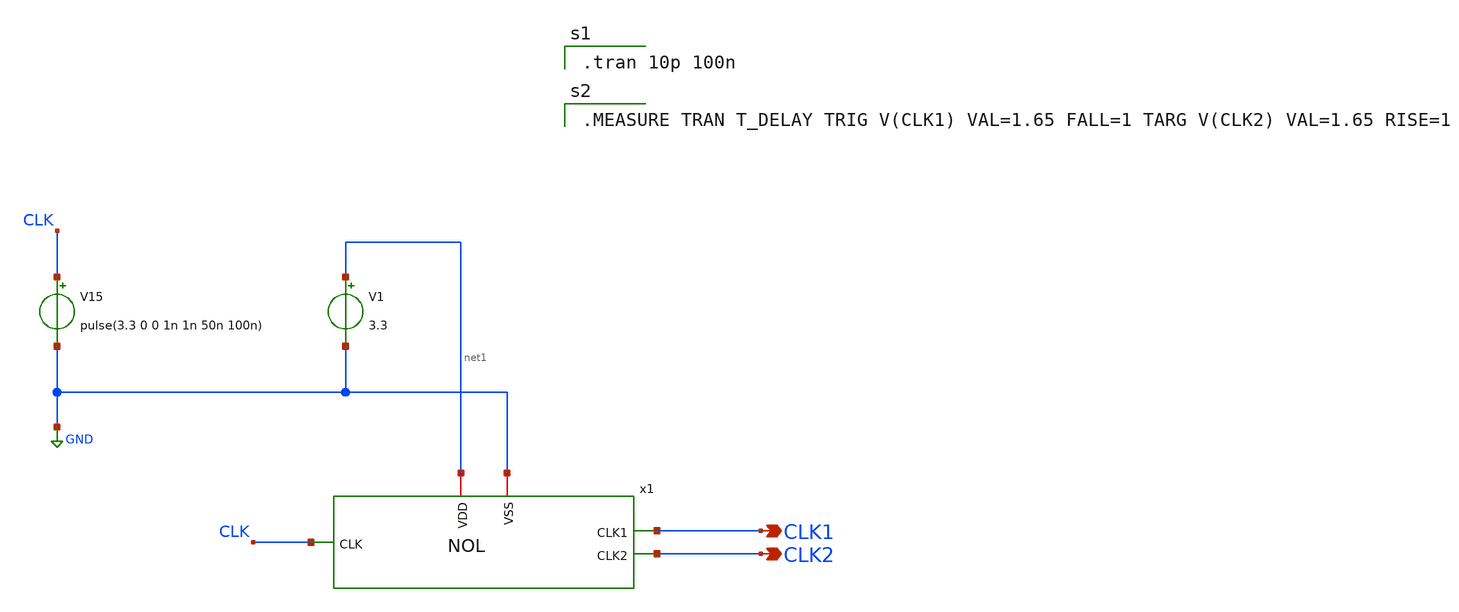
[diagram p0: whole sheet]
** sch_path: NOL_sim.sch
**.subckt NOL_sim CLK1 CLK2
*.opin CLK1
*.opin CLK2
x1 net1 CLK CLK1 GND CLK2 NOL
V15 CLK GND pulse(3.3 0 0 1n 1n 50n 100n)
V1 net1 GND 3.3
**** begin user architecture code

.tran 10p 100n


.MEASURE TRAN T_DELAY TRIG V(CLK1) VAL=1.65 FALL=1 TARG V(CLK2) VAL=1.65 RISE=1

**** end user architecture code
**.ends

* expanding   symbol:  C:/Users/ISLab2/Documents/minimal_LR/NOL.sym # of pins=5
** sym_path: NOL.sym
** sch_path: NOL.sch
.subckt NOL VDD CLK CLK1 VSS CLK2
*.ipin CLK
*.opin CLK1
*.opin CLK2
*.iopin VDD
*.iopin VSS
x3 VDD net1 CLK VSS INV
x1 VDD CLK net9 CLK2 VSS NOR
x2 VDD CLK1 net2 net1 VSS NOR
x4 VDD net3 net2 VSS INV
x5 VDD net4 net3 VSS INV
x6 VDD net5 net4 VSS INV
x7 VDD net17 net5 VSS INV
x8 VDD net6 net9 VSS INV
x9 VDD net7 net6 VSS INV
x10 VDD net8 net7 VSS INV
x11 VDD net13 net8 VSS INV
x12 VDD net10 net13 VSS INV
x13 VDD net11 net10 VSS INV
x14 VDD net12 net11 VSS INV
x15 VDD net32 net12 VSS INV
x16 VDD net14 net17 VSS INV
x17 VDD net15 net14 VSS INV
x18 VDD net16 net15 VSS INV
x19 VDD net33 net16 VSS INV
x20 VDD net18 net33 VSS INV
x21 VDD net19 net18 VSS INV
x22 VDD net20 net19 VSS INV
x23 VDD net24 net20 VSS INV
x24 VDD net21 net24 VSS INV
x25 VDD net22 net21 VSS INV
x26 VDD net23 net22 VSS INV
x27 VDD CLK2 net23 VSS INV
x28 VDD net25 net32 VSS INV
x29 VDD net26 net25 VSS INV
x30 VDD net27 net26 VSS INV
x31 VDD net31 net27 VSS INV
x32 VDD net28 net31 VSS INV
x33 VDD net29 net28 VSS INV
x34 VDD net30 net29 VSS INV
x35 VDD CLK1 net30 VSS INV
.ends


* expanding   symbol:  C:/Users/ISLab2/Documents/minimal_LR/INV.sym # of pins=4
** sym_path: INV.sym
** sch_path: INV.sch
.subckt INV VDD OUT IN VSS
*.opin OUT
*.ipin IN
*.iopin VDD
*.iopin VSS
M2 OUT IN VDD VDD pch w=10u l=0.35u as=0 ps=0 ad=0 pd=0 m=1
M1 OUT IN VSS VSS nch w=5u l=0.35u as=0 ps=0 ad=0 pd=0 m=1
.ends


* expanding   symbol:  C:/Users/ISLab2/Documents/minimal_LR/NOR.sym # of pins=5
** sym_path: NOR.sym
** sch_path: NOR.sch
.subckt NOR VDD A Y B VSS
*.iopin VDD
*.ipin A
*.ipin B
*.iopin VSS
*.opin Y
M1 Y A VSS VSS nch w=3.5u l=0.35u as=0 ps=0 ad=0 pd=0 m=1
M2 net1 A VDD VDD pch w=3.5u l=0.35u as=0 ps=0 ad=0 pd=0 m=1
M3 Y B net1 VDD pch w=3.5u l=0.35u as=0 ps=0 ad=0 pd=0 m=1
M4 Y B VSS VSS nch w=3.5u l=0.35u as=0 ps=0 ad=0 pd=0 m=1
**** begin user architecture code


.include C:/Users/ISLab2/Documents/minimal_LR/minimal.txt

**** end user architecture code
.ends

.GLOBAL GND
.end
